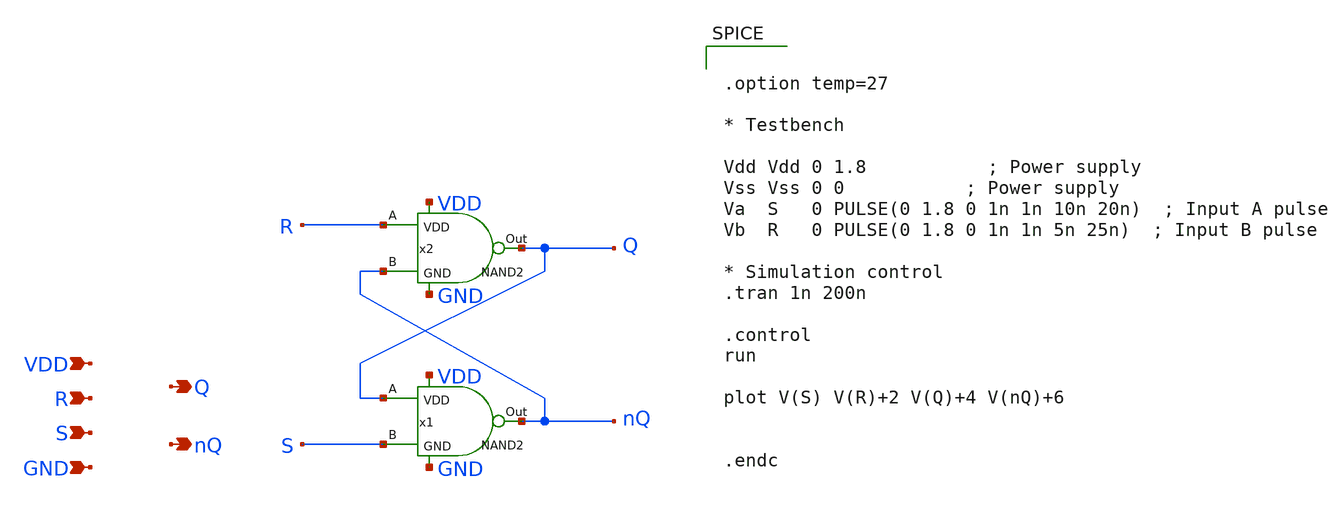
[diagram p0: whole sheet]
** sch_path: src/SR_NAND2.sch
**.subckt SR_NAND2 Q R S VDD GND nQ
*.opin Q
*.ipin R
*.ipin S
*.ipin VDD
*.ipin GND
*.opin nQ
x1 Q nQ S VDD GND NAND2
x2 R Q nQ VDD GND NAND2
**** begin user architecture code

** opencircuitdesign pdks install
.lib $::SKYWATER_MODELS/sky130.lib.spice tt




.option temp=27

* Testbench

Vdd Vdd 0 1.8           ; Power supply
Vss Vss 0 0           ; Power supply
Va  S   0 PULSE(0 1.8 0 1n 1n 10n 20n)  ; Input A pulse
Vb  R   0 PULSE(0 1.8 0 1n 1n 5n 25n)  ; Input B pulse

* Simulation control
.tran 1n 200n

.control
run

plot V(S) V(R)+2 V(Q)+4 V(nQ)+6


.endc


**** end user architecture code
**.ends

* expanding   symbol:  /foss/designs/PLL2_4/src/NAND2.sym # of pins=5
** sym_path: src/NAND2.sym
** sch_path: src/NAND2.sch
.subckt NAND2 A Out B VDD GND
*.opin Out
*.ipin A
*.ipin B
*.ipin VDD
*.ipin GND
XM1 Out A VDD VDD sky130_fd_pr__pfet_01v8 L=1 W=1 nf=1 ad='int((1 + 1)/2) * 1 / 1 * 0.29' as='int((1 + 2)/2) * 1 / 1 * 0.29'
+ pd='2*int((1 + 1)/2) * (1 / 1 + 0.29)' ps='2*int((1 + 2)/2) * (1 / 1 + 0.29)' nrd='0.29 / 1 ' nrs='0.29 / 1 '
+ sa=0 sb=0 sd=0 mult=1 m=1
XM3 Out B VDD VDD sky130_fd_pr__pfet_01v8 L=1 W=1 nf=1 ad='int((1 + 1)/2) * 1 / 1 * 0.29' as='int((1 + 2)/2) * 1 / 1 * 0.29'
+ pd='2*int((1 + 1)/2) * (1 / 1 + 0.29)' ps='2*int((1 + 2)/2) * (1 / 1 + 0.29)' nrd='0.29 / 1 ' nrs='0.29 / 1 '
+ sa=0 sb=0 sd=0 mult=1 m=1
XM4 net1 B GND GND sky130_fd_pr__nfet_01v8 L=1 W=1 nf=1 ad='int((1 + 1)/2) * 1 / 1 * 0.29' as='int((1 + 2)/2) * 1 / 1 * 0.29'
+ pd='2*int((1 + 1)/2) * (1 / 1 + 0.29)' ps='2*int((1 + 2)/2) * (1 / 1 + 0.29)' nrd='0.29 / 1 ' nrs='0.29 / 1 '
+ sa=0 sb=0 sd=0 mult=1 m=1
XM5 Out A net1 GND sky130_fd_pr__nfet_01v8 L=1 W=1 nf=1 ad='int((1 + 1)/2) * 1 / 1 * 0.29' as='int((1 + 2)/2) * 1 / 1 * 0.29'
+ pd='2*int((1 + 1)/2) * (1 / 1 + 0.29)' ps='2*int((1 + 2)/2) * (1 / 1 + 0.29)' nrd='0.29 / 1 ' nrs='0.29 / 1 '
+ sa=0 sb=0 sd=0 mult=1 m=1
.ends

.end
